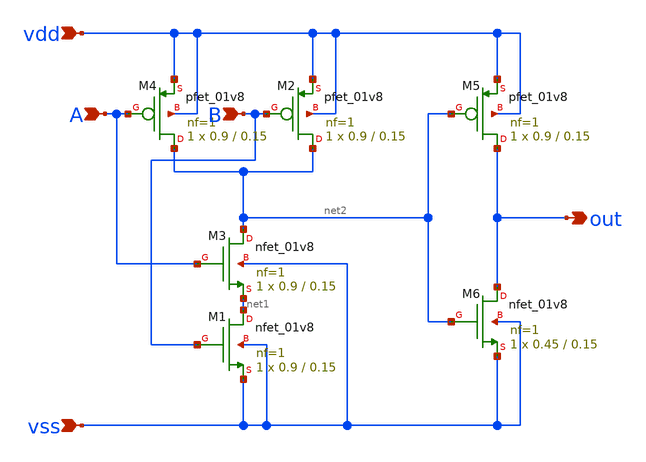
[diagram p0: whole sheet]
** sch_path: track_vlsi/ledesma/sch/and.sch
**.subckt and out vdd A B vss
*.opin out
*.ipin vdd
*.ipin A
*.ipin B
*.ipin vss
XM1 net1 B vss vss sky130_fd_pr__nfet_01v8 L=0.15 W=0.9 nf=1 ad='int((nf+1)/2) * W/nf * 0.29' as='int((nf+2)/2) * W/nf * 0.29'
+ pd='2*int((nf+1)/2) * (W/nf + 0.29)' ps='2*int((nf+2)/2) * (W/nf + 0.29)' nrd='0.29 / W' nrs='0.29 / W'
+ sa=0 sb=0 sd=0 mult=1 m=1
XM2 net2 B vdd vdd sky130_fd_pr__pfet_01v8 L=0.15 W=0.9 nf=1 ad='int((nf+1)/2) * W/nf * 0.29' as='int((nf+2)/2) * W/nf * 0.29'
+ pd='2*int((nf+1)/2) * (W/nf + 0.29)' ps='2*int((nf+2)/2) * (W/nf + 0.29)' nrd='0.29 / W' nrs='0.29 / W'
+ sa=0 sb=0 sd=0 mult=1 m=1
XM3 net2 A net1 vss sky130_fd_pr__nfet_01v8 L=0.15 W=0.9 nf=1 ad='int((nf+1)/2) * W/nf * 0.29' as='int((nf+2)/2) * W/nf * 0.29'
+ pd='2*int((nf+1)/2) * (W/nf + 0.29)' ps='2*int((nf+2)/2) * (W/nf + 0.29)' nrd='0.29 / W' nrs='0.29 / W'
+ sa=0 sb=0 sd=0 mult=1 m=1
XM4 net2 A vdd vdd sky130_fd_pr__pfet_01v8 L=0.15 W=0.9 nf=1 ad='int((nf+1)/2) * W/nf * 0.29' as='int((nf+2)/2) * W/nf * 0.29'
+ pd='2*int((nf+1)/2) * (W/nf + 0.29)' ps='2*int((nf+2)/2) * (W/nf + 0.29)' nrd='0.29 / W' nrs='0.29 / W'
+ sa=0 sb=0 sd=0 mult=1 m=1
XM5 out net2 vdd vdd sky130_fd_pr__pfet_01v8 L=0.15 W=0.9 nf=1 ad='int((nf+1)/2) * W/nf * 0.29' as='int((nf+2)/2) * W/nf * 0.29'
+ pd='2*int((nf+1)/2) * (W/nf + 0.29)' ps='2*int((nf+2)/2) * (W/nf + 0.29)' nrd='0.29 / W' nrs='0.29 / W'
+ sa=0 sb=0 sd=0 mult=1 m=1
XM6 out net2 vss vss sky130_fd_pr__nfet_01v8 L=0.15 W=0.45 nf=1 ad='int((nf+1)/2) * W/nf * 0.29' as='int((nf+2)/2) * W/nf * 0.29'
+ pd='2*int((nf+1)/2) * (W/nf + 0.29)' ps='2*int((nf+2)/2) * (W/nf + 0.29)' nrd='0.29 / W' nrs='0.29 / W'
+ sa=0 sb=0 sd=0 mult=1 m=1
**.ends
.end
